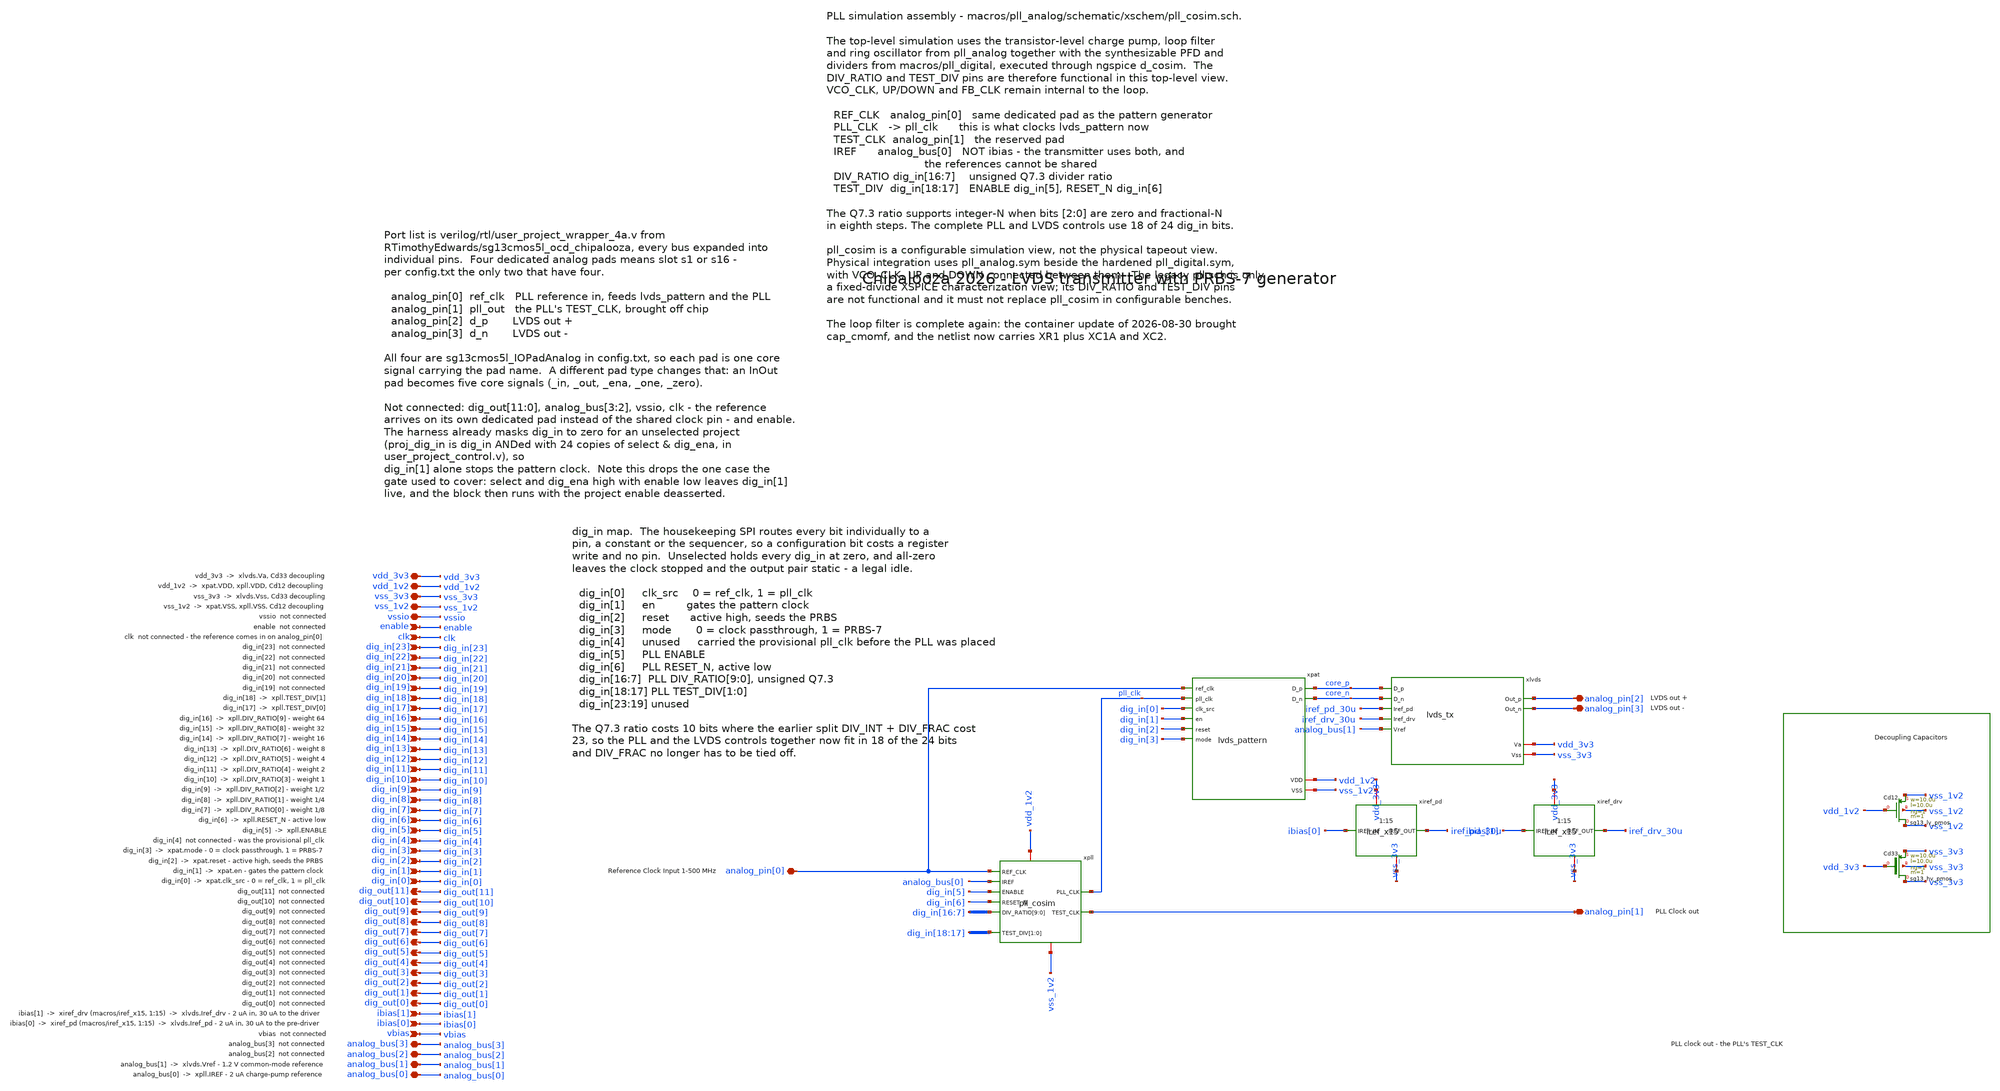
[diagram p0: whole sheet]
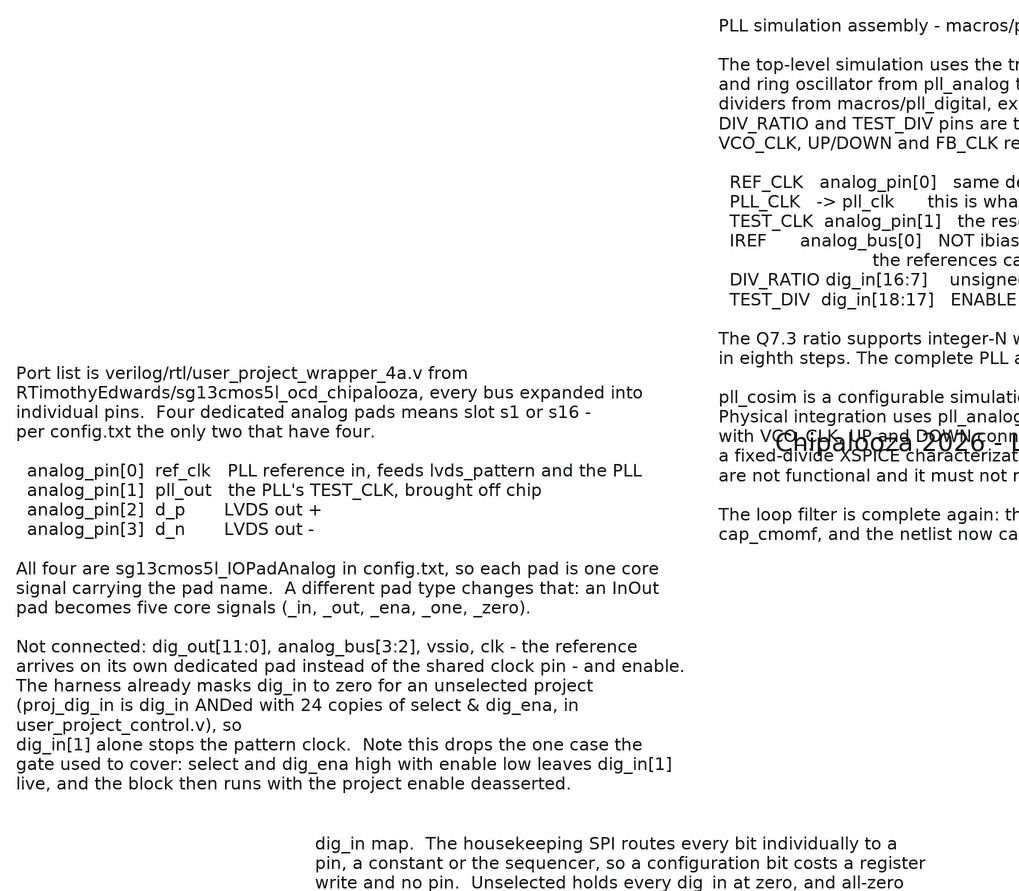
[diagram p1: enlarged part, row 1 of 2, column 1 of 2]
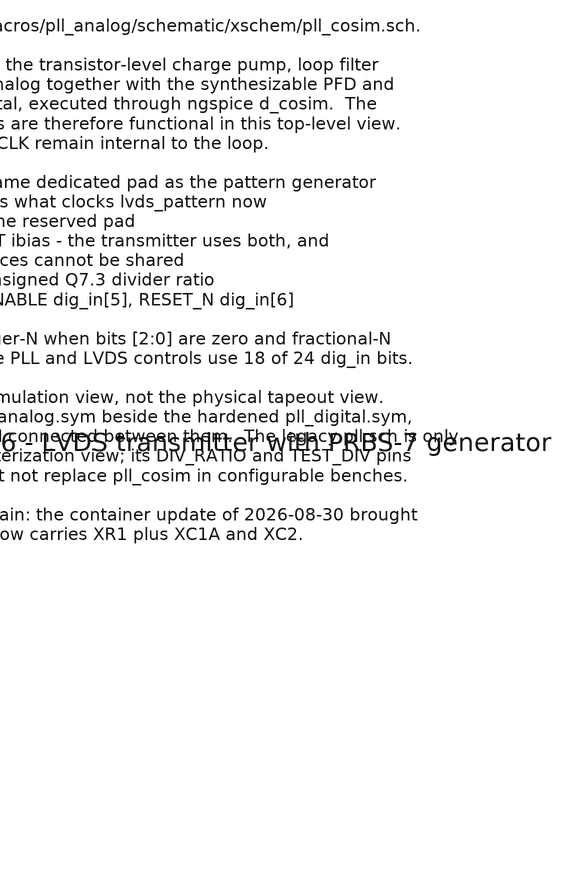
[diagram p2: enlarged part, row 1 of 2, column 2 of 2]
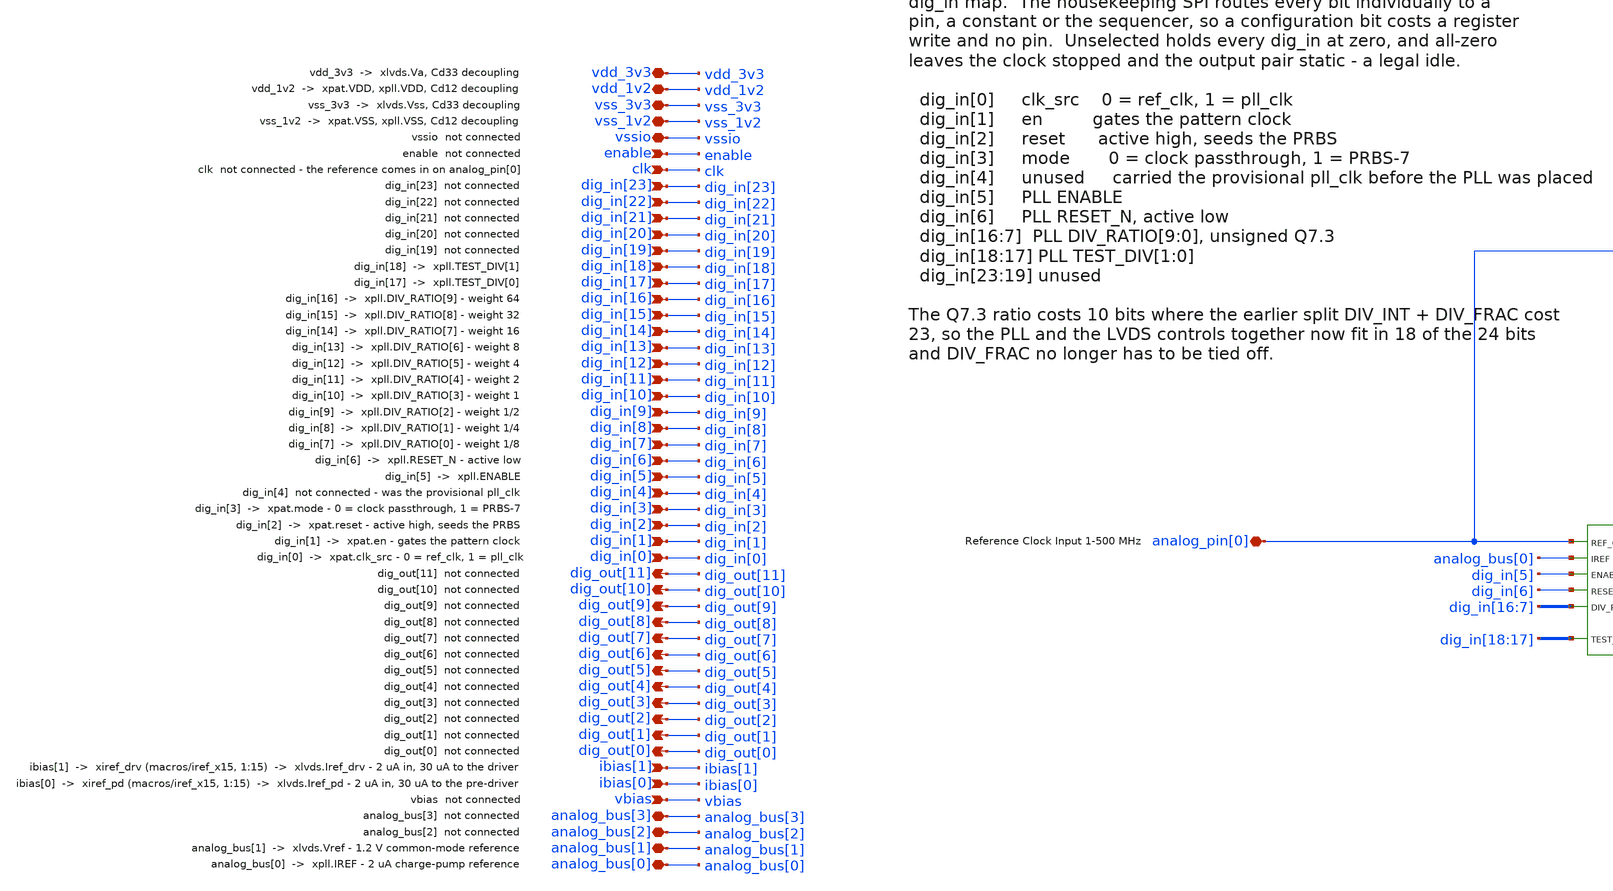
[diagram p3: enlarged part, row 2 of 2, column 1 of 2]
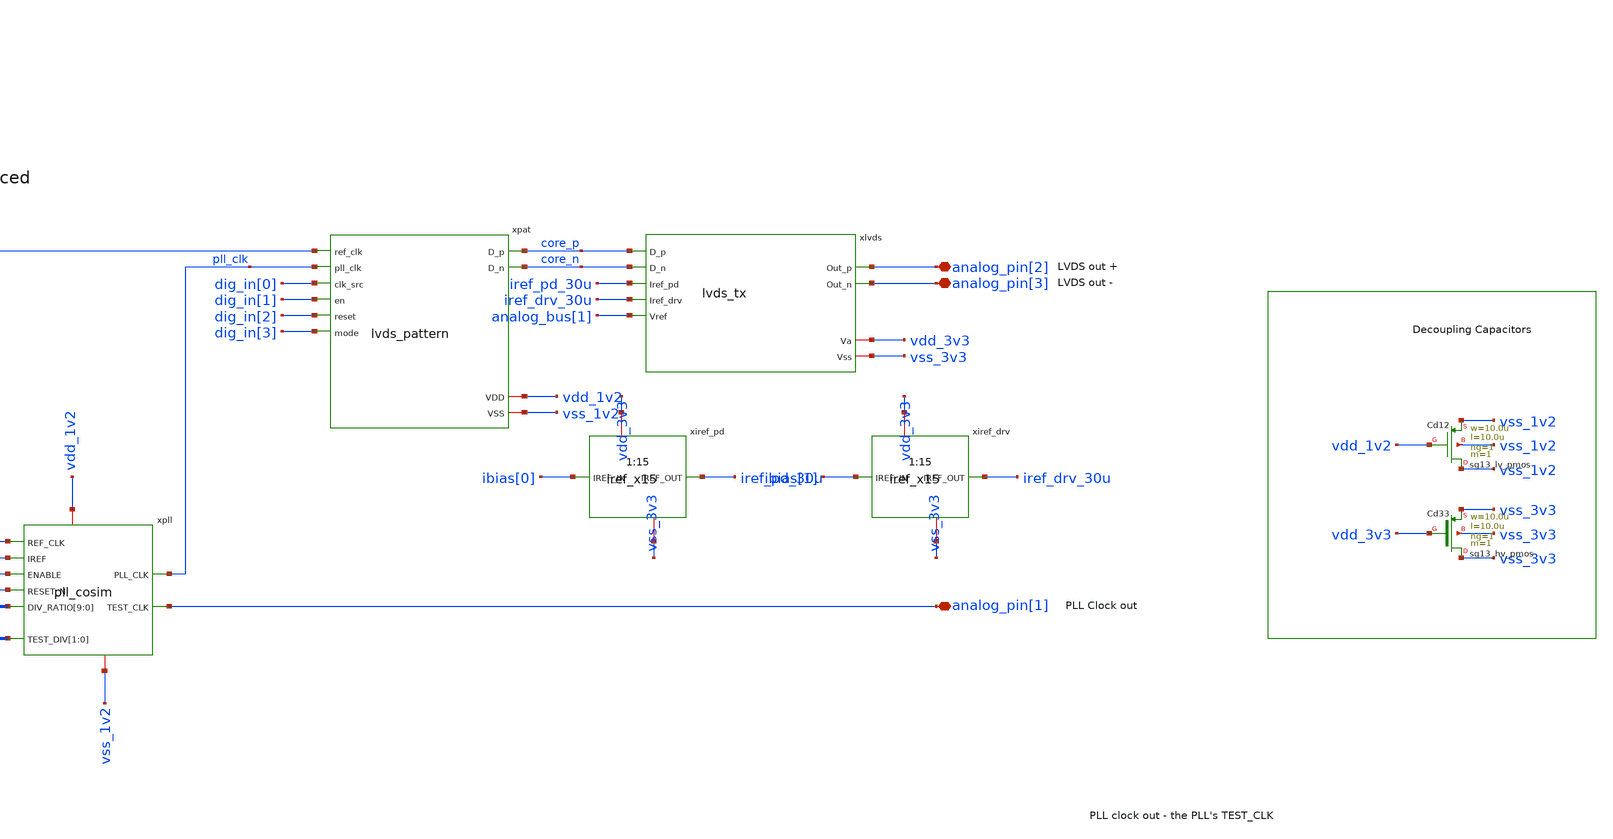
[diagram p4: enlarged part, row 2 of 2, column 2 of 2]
** sch_path: schematic/xschem/sg13cmos5l_chipalooza_analog_project.sch
**.subckt sg13cmos5l_chipalooza_analog_project vdd_3v3 vdd_1v2 vss_3v3 vss_1v2 vssio enable clk
*+ dig_in[23] dig_in[22] dig_in[21] dig_in[20] dig_in[19] dig_in[18] dig_in[17] dig_in[16] dig_in[15] dig_in[14]
*+ dig_in[13] dig_in[12] dig_in[11] dig_in[10] dig_in[9] dig_in[8] dig_in[7] dig_in[6] dig_in[5] dig_in[4]
*+ dig_in[3] dig_in[2] dig_in[1] dig_in[0] dig_out[11] dig_out[10] dig_out[9] dig_out[8] dig_out[7] dig_out[6]
*+ dig_out[5] dig_out[4] dig_out[3] dig_out[2] dig_out[1] dig_out[0] analog_pin[3] analog_pin[2] analog_pin[1]
*+ analog_pin[0] ibias[1] ibias[0] vbias analog_bus[3] analog_bus[2] analog_bus[1] analog_bus[0]
*.iopin vdd_3v3
*.iopin vdd_1v2
*.iopin vss_3v3
*.iopin vss_1v2
*.iopin vssio
*.ipin enable
*.ipin clk
*.ipin dig_in[23]
*.ipin dig_in[22]
*.ipin dig_in[21]
*.ipin dig_in[20]
*.ipin dig_in[19]
*.ipin dig_in[18]
*.ipin dig_in[17]
*.ipin dig_in[16]
*.ipin dig_in[15]
*.ipin dig_in[14]
*.ipin dig_in[13]
*.ipin dig_in[12]
*.ipin dig_in[11]
*.ipin dig_in[10]
*.ipin dig_in[9]
*.ipin dig_in[8]
*.ipin dig_in[7]
*.ipin dig_in[6]
*.ipin dig_in[5]
*.ipin dig_in[4]
*.ipin dig_in[3]
*.ipin dig_in[2]
*.ipin dig_in[1]
*.ipin dig_in[0]
*.opin dig_out[11]
*.opin dig_out[10]
*.opin dig_out[9]
*.opin dig_out[8]
*.opin dig_out[7]
*.opin dig_out[6]
*.opin dig_out[5]
*.opin dig_out[4]
*.opin dig_out[3]
*.opin dig_out[2]
*.opin dig_out[1]
*.opin dig_out[0]
*.iopin analog_pin[3]
*.iopin analog_pin[2]
*.iopin analog_pin[1]
*.iopin analog_pin[0]
*.ipin ibias[1]
*.ipin ibias[0]
*.ipin vbias
*.iopin analog_bus[3]
*.iopin analog_bus[2]
*.iopin analog_bus[1]
*.iopin analog_bus[0]
xpat analog_pin[0] pll_clk dig_in[0] dig_in[1] dig_in[2] dig_in[3] core_p core_n vdd_1v2 vss_1v2
+ lvds_pattern
xlvds core_p core_n iref_pd_30u iref_drv_30u analog_bus[1] vdd_3v3 analog_pin[2] analog_pin[3]
+ vss_3v3 lvds_tx
xiref_pd ibias[0] iref_pd_30u vdd_3v3 vss_3v3 iref_x15
xiref_drv ibias[1] iref_drv_30u vdd_3v3 vss_3v3 iref_x15
XCd12 vss_1v2 vdd_1v2 vss_1v2 vss_1v2 sg13_lv_pmos w=10.0u l=10.0u ng=1 m=1 mm_ok=1
XCd33 vss_3v3 vdd_3v3 vss_3v3 vss_3v3 sg13_hv_pmos w=10.0u l=10.0u ng=1 m=1 mm_ok=1
xpll analog_pin[0] analog_bus[0] dig_in[5] dig_in[6] dig_in[16] dig_in[15] dig_in[14] dig_in[13]
+ dig_in[12] dig_in[11] dig_in[10] dig_in[9] dig_in[8] dig_in[7] dig_in[18] dig_in[17] pll_clk analog_pin[1]
+ vdd_1v2 vss_1v2 pll_cosim
**.ends
.end
